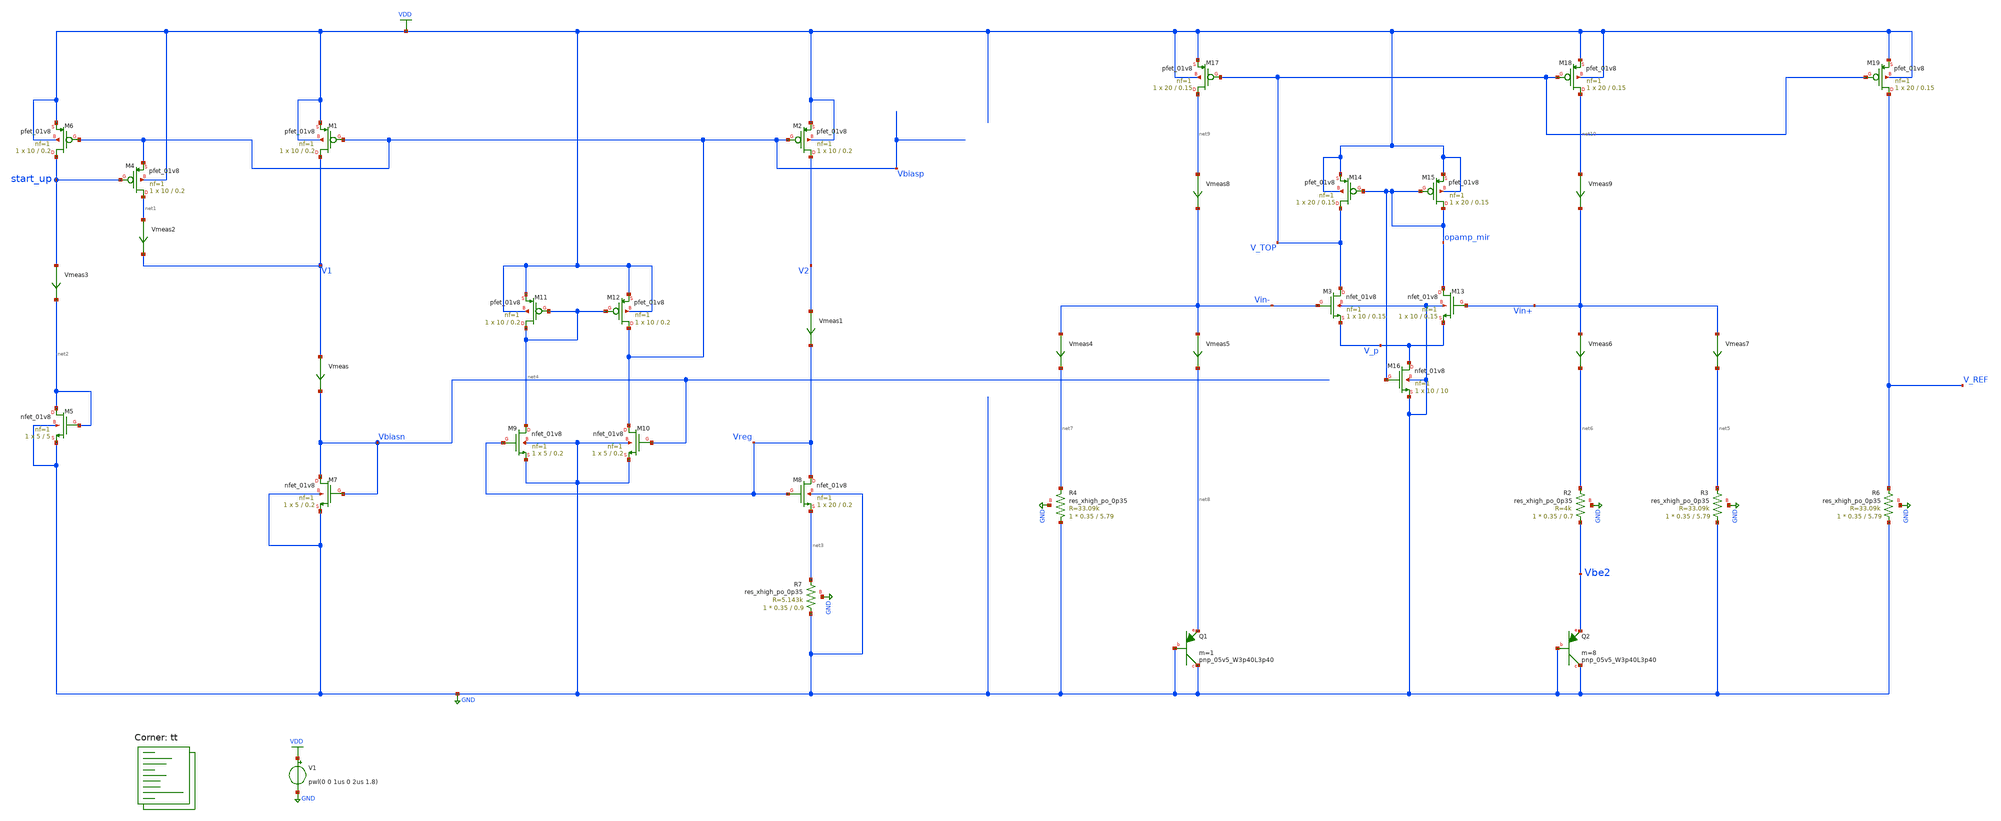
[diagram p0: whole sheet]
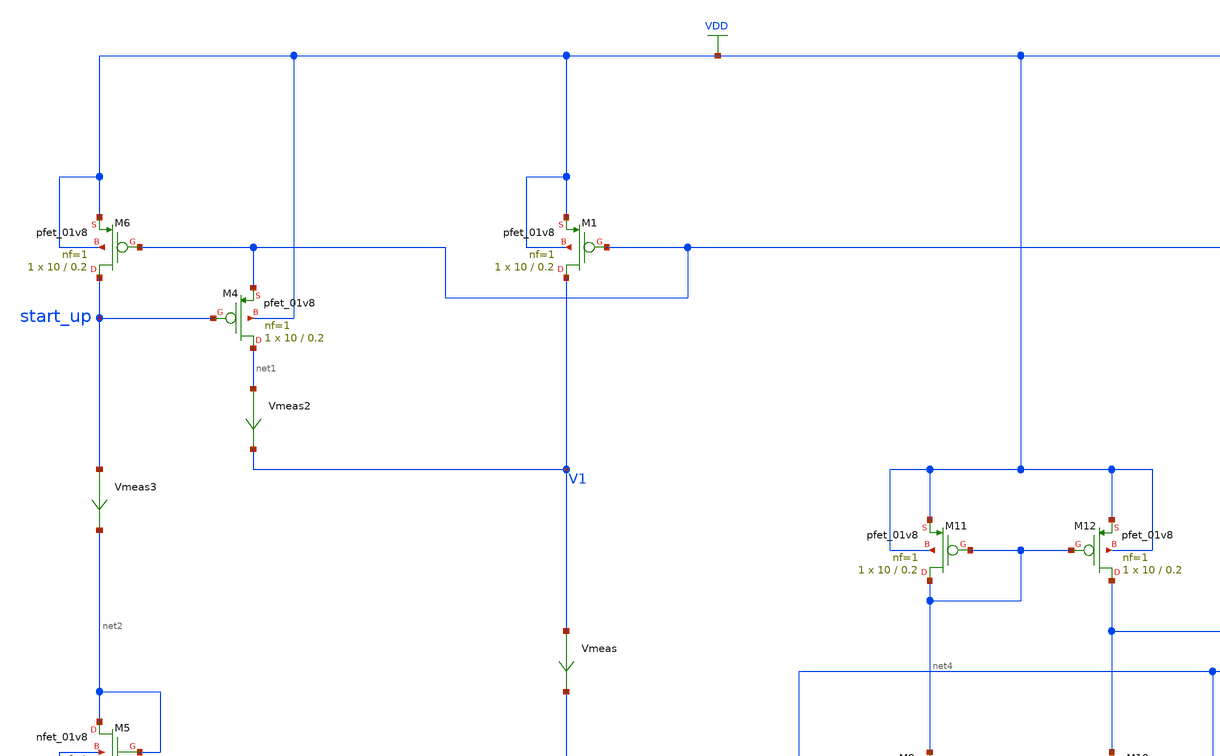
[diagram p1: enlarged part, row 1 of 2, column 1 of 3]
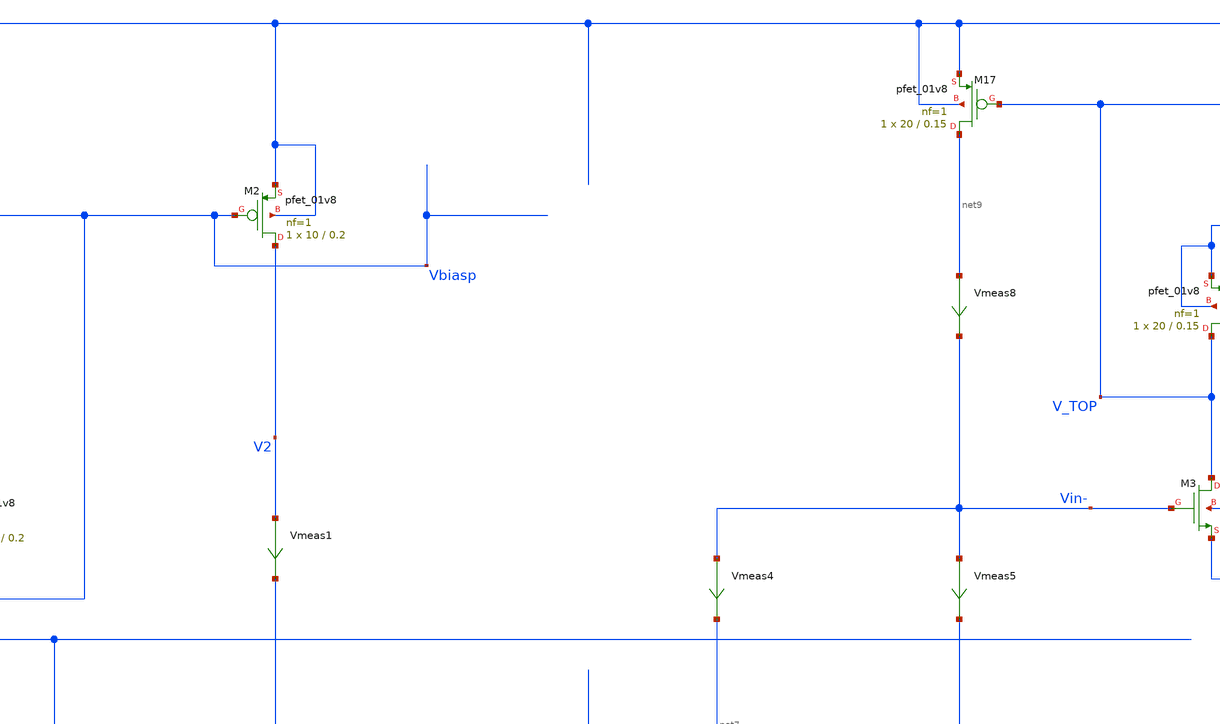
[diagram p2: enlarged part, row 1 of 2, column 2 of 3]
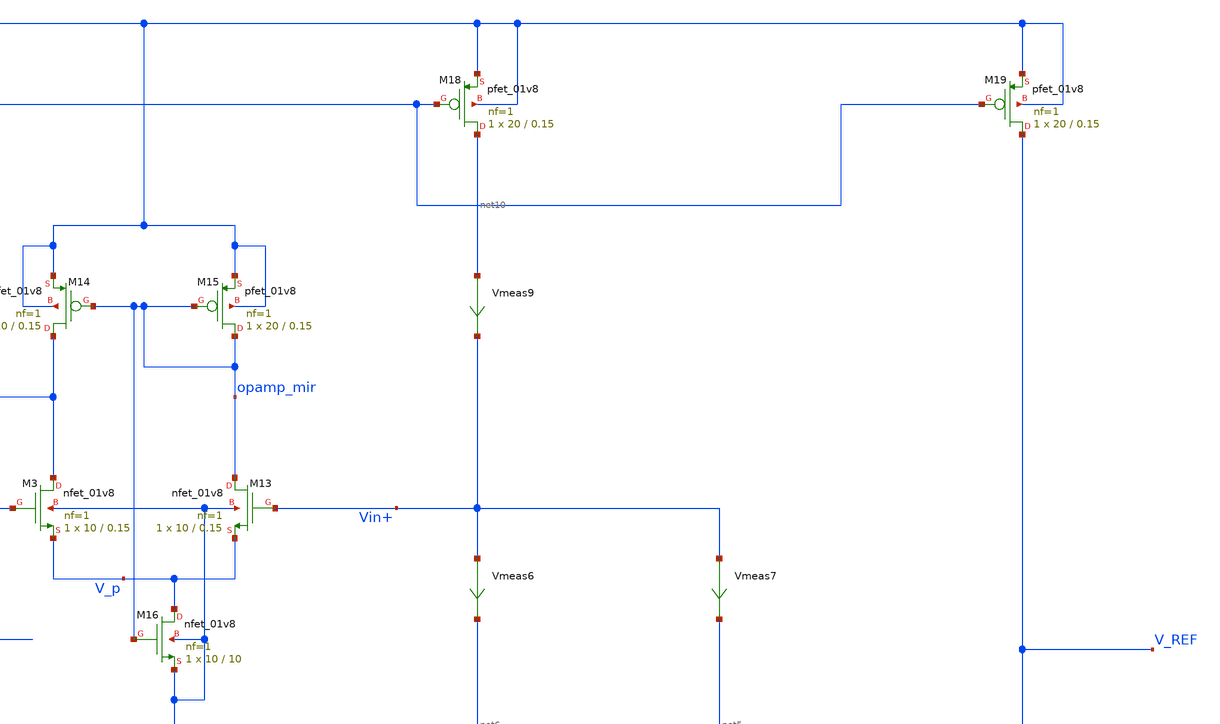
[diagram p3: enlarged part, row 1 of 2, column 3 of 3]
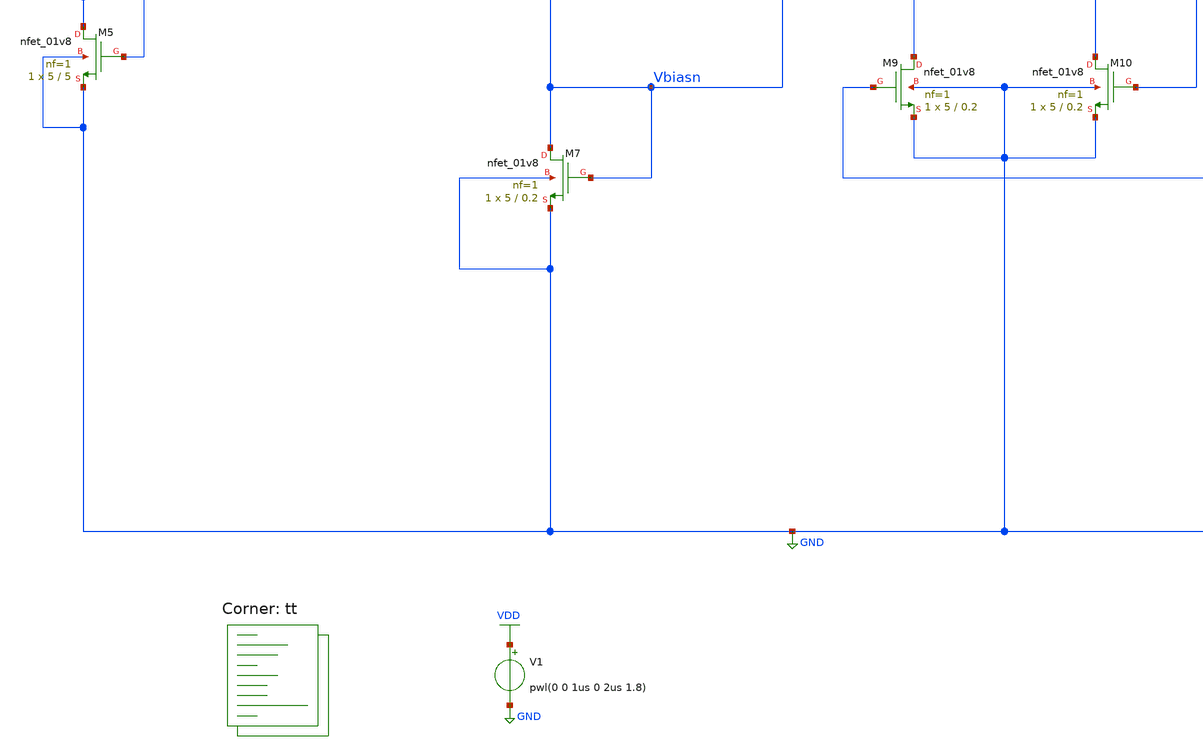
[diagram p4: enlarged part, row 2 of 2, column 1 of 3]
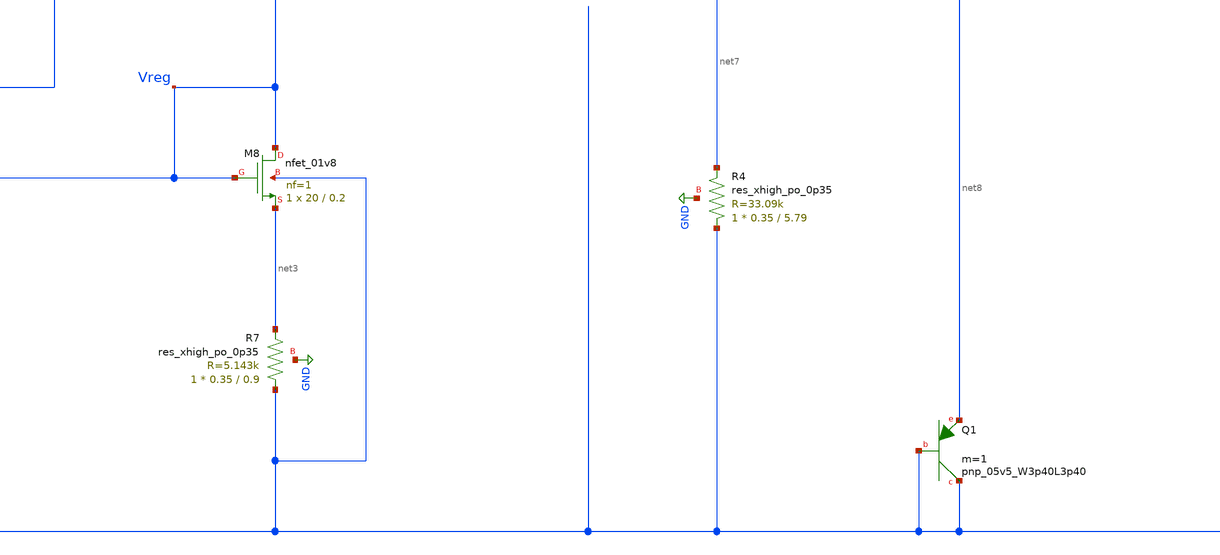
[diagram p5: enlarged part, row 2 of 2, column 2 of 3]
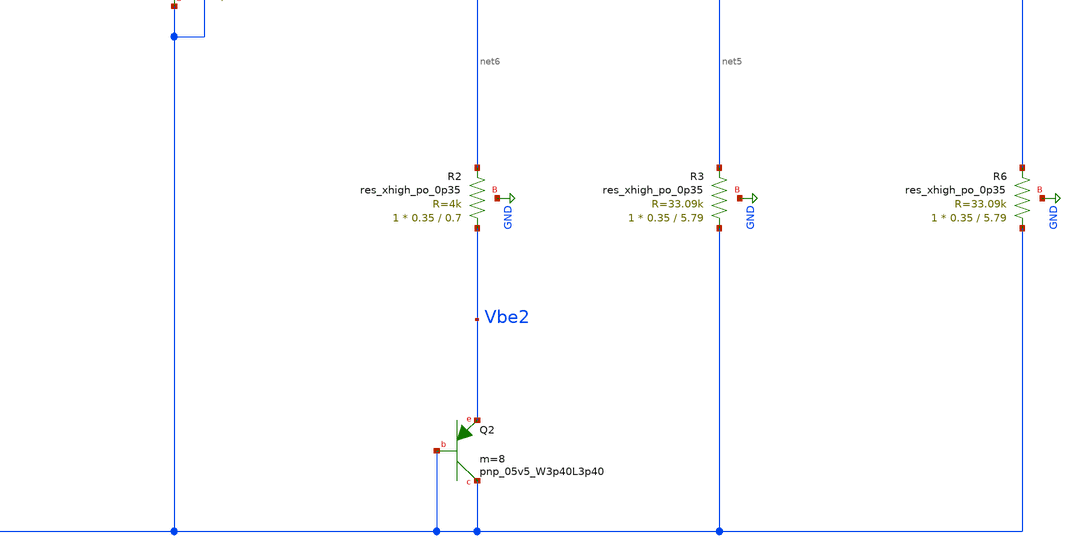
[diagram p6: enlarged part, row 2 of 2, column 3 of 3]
** sch_path: projects/bandgapref/xschem_ngspice/new_files/tb_low_voltage_BGR_8.sch
**.subckt tb_low_voltage_BGR_8
V1 VDD GND pwl(0 0 1us 0 2us 1.8)
XM1 V1 Vbiasp VDD VDD sky130_fd_pr__pfet_01v8 L=0.2 W=10 nf=1 ad='int((nf+1)/2) * W/nf * 0.29' as='int((nf+2)/2) * W/nf * 0.29'
+ pd='2*int((nf+1)/2) * (W/nf + 0.29)' ps='2*int((nf+2)/2) * (W/nf + 0.29)' nrd='0.29 / W' nrs='0.29 / W'
+ sa=0 sb=0 sd=0 mult=1 m=1
XM2 V2 Vbiasp VDD VDD sky130_fd_pr__pfet_01v8 L=0.2 W=10 nf=1 ad='int((nf+1)/2) * W/nf * 0.29' as='int((nf+2)/2) * W/nf * 0.29'
+ pd='2*int((nf+1)/2) * (W/nf + 0.29)' ps='2*int((nf+2)/2) * (W/nf + 0.29)' nrd='0.29 / W' nrs='0.29 / W'
+ sa=0 sb=0 sd=0 mult=1 m=1
Vmeas V1 Vbiasn 0
.save i(vmeas)
Vmeas1 V2 Vreg 0
.save i(vmeas1)
XM5 net2 net2 GND GND sky130_fd_pr__nfet_01v8 L=5 W=5 nf=1 ad='int((nf+1)/2) * W/nf * 0.29' as='int((nf+2)/2) * W/nf * 0.29'
+ pd='2*int((nf+1)/2) * (W/nf + 0.29)' ps='2*int((nf+2)/2) * (W/nf + 0.29)' nrd='0.29 / W' nrs='0.29 / W'
+ sa=0 sb=0 sd=0 mult=1 m=1
XM6 start_up Vbiasp VDD VDD sky130_fd_pr__pfet_01v8 L=0.2 W=10 nf=1 ad='int((nf+1)/2) * W/nf * 0.29'
+ as='int((nf+2)/2) * W/nf * 0.29' pd='2*int((nf+1)/2) * (W/nf + 0.29)' ps='2*int((nf+2)/2) * (W/nf + 0.29)'
+ nrd='0.29 / W' nrs='0.29 / W' sa=0 sb=0 sd=0 mult=1 m=1
XM4 net1 start_up Vbiasp VDD sky130_fd_pr__pfet_01v8 L=0.2 W=10 nf=1 ad='int((nf+1)/2) * W/nf * 0.29'
+ as='int((nf+2)/2) * W/nf * 0.29' pd='2*int((nf+1)/2) * (W/nf + 0.29)' ps='2*int((nf+2)/2) * (W/nf + 0.29)'
+ nrd='0.29 / W' nrs='0.29 / W' sa=0 sb=0 sd=0 mult=1 m=1
XM7 Vbiasn Vbiasn GND GND sky130_fd_pr__nfet_01v8 L=0.2 W=5 nf=1 ad='int((nf+1)/2) * W/nf * 0.29' as='int((nf+2)/2) * W/nf * 0.29'
+ pd='2*int((nf+1)/2) * (W/nf + 0.29)' ps='2*int((nf+2)/2) * (W/nf + 0.29)' nrd='0.29 / W' nrs='0.29 / W'
+ sa=0 sb=0 sd=0 mult=1 m=1
XM8 Vreg Vreg net3 GND sky130_fd_pr__nfet_01v8 L=0.2 W=20 nf=1 ad='int((nf+1)/2) * W/nf * 0.29' as='int((nf+2)/2) * W/nf * 0.29'
+ pd='2*int((nf+1)/2) * (W/nf + 0.29)' ps='2*int((nf+2)/2) * (W/nf + 0.29)' nrd='0.29 / W' nrs='0.29 / W'
+ sa=0 sb=0 sd=0 mult=1 m=1
Vmeas2 net1 V1 0
.save i(vmeas2)
Vmeas3 start_up net2 0
.save i(vmeas3)
XM9 net4 Vreg GND GND sky130_fd_pr__nfet_01v8 L=0.2 W=5 nf=1 ad='int((nf+1)/2) * W/nf * 0.29' as='int((nf+2)/2) * W/nf * 0.29'
+ pd='2*int((nf+1)/2) * (W/nf + 0.29)' ps='2*int((nf+2)/2) * (W/nf + 0.29)' nrd='0.29 / W' nrs='0.29 / W'
+ sa=0 sb=0 sd=0 mult=1 m=1
XM10 Vbiasp Vbiasn GND GND sky130_fd_pr__nfet_01v8 L=0.2 W=5 nf=1 ad='int((nf+1)/2) * W/nf * 0.29' as='int((nf+2)/2) * W/nf * 0.29'
+ pd='2*int((nf+1)/2) * (W/nf + 0.29)' ps='2*int((nf+2)/2) * (W/nf + 0.29)' nrd='0.29 / W' nrs='0.29 / W'
+ sa=0 sb=0 sd=0 mult=1 m=1
XM11 net4 net4 VDD VDD sky130_fd_pr__pfet_01v8 L=0.2 W=10 nf=1 ad='int((nf+1)/2) * W/nf * 0.29' as='int((nf+2)/2) * W/nf * 0.29'
+ pd='2*int((nf+1)/2) * (W/nf + 0.29)' ps='2*int((nf+2)/2) * (W/nf + 0.29)' nrd='0.29 / W' nrs='0.29 / W'
+ sa=0 sb=0 sd=0 mult=1 m=1
XM12 Vbiasp net4 VDD VDD sky130_fd_pr__pfet_01v8 L=0.2 W=10 nf=1 ad='int((nf+1)/2) * W/nf * 0.29' as='int((nf+2)/2) * W/nf * 0.29'
+ pd='2*int((nf+1)/2) * (W/nf + 0.29)' ps='2*int((nf+2)/2) * (W/nf + 0.29)' nrd='0.29 / W' nrs='0.29 / W'
+ sa=0 sb=0 sd=0 mult=1 m=1
XM3 V_TOP Vin- V_p GND sky130_fd_pr__nfet_01v8 L=0.15 W=10 nf=1 ad='int((nf+1)/2) * W/nf * 0.29' as='int((nf+2)/2) * W/nf * 0.29'
+ pd='2*int((nf+1)/2) * (W/nf + 0.29)' ps='2*int((nf+2)/2) * (W/nf + 0.29)' nrd='0.29 / W' nrs='0.29 / W'
+ sa=0 sb=0 sd=0 mult=1 m=1
XM13 opamp_mir Vin+ V_p GND sky130_fd_pr__nfet_01v8 L=0.15 W=10 nf=1 ad='int((nf+1)/2) * W/nf * 0.29'
+ as='int((nf+2)/2) * W/nf * 0.29' pd='2*int((nf+1)/2) * (W/nf + 0.29)' ps='2*int((nf+2)/2) * (W/nf + 0.29)'
+ nrd='0.29 / W' nrs='0.29 / W' sa=0 sb=0 sd=0 mult=1 m=1
XM14 V_TOP opamp_mir VDD VDD sky130_fd_pr__pfet_01v8 L=0.15 W=20 nf=1 ad='int((nf+1)/2) * W/nf * 0.29'
+ as='int((nf+2)/2) * W/nf * 0.29' pd='2*int((nf+1)/2) * (W/nf + 0.29)' ps='2*int((nf+2)/2) * (W/nf + 0.29)'
+ nrd='0.29 / W' nrs='0.29 / W' sa=0 sb=0 sd=0 mult=1 m=1
XM15 opamp_mir opamp_mir VDD VDD sky130_fd_pr__pfet_01v8 L=0.15 W=20 nf=1 ad='int((nf+1)/2) * W/nf * 0.29'
+ as='int((nf+2)/2) * W/nf * 0.29' pd='2*int((nf+1)/2) * (W/nf + 0.29)' ps='2*int((nf+2)/2) * (W/nf + 0.29)'
+ nrd='0.29 / W' nrs='0.29 / W' sa=0 sb=0 sd=0 mult=1 m=1
XQ1 GND GND net8 sky130_fd_pr__pnp_05v5_W3p40L3p40 m=1
XQ2 GND GND Vbe2 sky130_fd_pr__pnp_05v5_W3p40L3p40 m=8
XR2 Vbe2 net6 GND sky130_fd_pr__res_xhigh_po_0p35 L=0.7 mult=1 m=1
XM17 net9 V_TOP VDD VDD sky130_fd_pr__pfet_01v8 L=0.15 W=20 nf=1 ad='int((nf+1)/2) * W/nf * 0.29' as='int((nf+2)/2) * W/nf * 0.29'
+ pd='2*int((nf+1)/2) * (W/nf + 0.29)' ps='2*int((nf+2)/2) * (W/nf + 0.29)' nrd='0.29 / W' nrs='0.29 / W'
+ sa=0 sb=0 sd=0 mult=1 m=1
XM18 net10 V_TOP VDD VDD sky130_fd_pr__pfet_01v8 L=0.15 W=20 nf=1 ad='int((nf+1)/2) * W/nf * 0.29' as='int((nf+2)/2) * W/nf * 0.29'
+ pd='2*int((nf+1)/2) * (W/nf + 0.29)' ps='2*int((nf+2)/2) * (W/nf + 0.29)' nrd='0.29 / W' nrs='0.29 / W'
+ sa=0 sb=0 sd=0 mult=1 m=1
XR3 GND net5 GND sky130_fd_pr__res_xhigh_po_0p35 L=5.79 mult=1 m=1
XR4 GND net7 GND sky130_fd_pr__res_xhigh_po_0p35 L=5.79 mult=1 m=1
XM19 V_REF V_TOP VDD VDD sky130_fd_pr__pfet_01v8 L=0.15 W=20 nf=1 ad='int((nf+1)/2) * W/nf * 0.29' as='int((nf+2)/2) * W/nf * 0.29'
+ pd='2*int((nf+1)/2) * (W/nf + 0.29)' ps='2*int((nf+2)/2) * (W/nf + 0.29)' nrd='0.29 / W' nrs='0.29 / W'
+ sa=0 sb=0 sd=0 mult=1 m=1
XR6 GND V_REF GND sky130_fd_pr__res_xhigh_po_0p35 L=5.79 mult=1 m=1
Vmeas4 Vin- net7 0
.save i(vmeas4)
Vmeas5 Vin- net8 0
.save i(vmeas5)
Vmeas6 Vin+ net6 0
.save i(vmeas6)
Vmeas7 Vin+ net5 0
.save i(vmeas7)
Vmeas8 net9 Vin- 0
.save i(vmeas8)
Vmeas9 net10 Vin+ 0
.save i(vmeas9)
XR7 GND net3 GND sky130_fd_pr__res_xhigh_po_0p35 L=0.9 mult=1 m=1
XM16 V_p opamp_mir GND GND sky130_fd_pr__nfet_01v8 L=10 W=10 nf=1 ad='int((nf+1)/2) * W/nf * 0.29' as='int((nf+2)/2) * W/nf * 0.29'
+ pd='2*int((nf+1)/2) * (W/nf + 0.29)' ps='2*int((nf+2)/2) * (W/nf + 0.29)' nrd='0.29 / W' nrs='0.29 / W'
+ sa=0 sb=0 sd=0 mult=1 m=1
**** begin user architecture code
.lib $::SKYWATER_MODELS/sky130.lib.spice tt



.option method=gear
.option wnflag=1
.option savecurrents
* .temp =140

.save @m.xm1.msky130_fd_pr__pfet_01v8[gm] @m.xm1.msky130_fd_pr__pfet_01v8[vth] @m.xm1.msky130_fd_pr__pfet_01v8[vgs] @m.xm1.msky130_fd_pr__pfet_01v8[vds] @m.xm2.msky130_fd_pr__pfet_01v8[gm] @m.xm2.msky130_fd_pr__pfet_01v8[vth] @m.xm2.msky130_fd_pr__pfet_01v8[vgs] @m.xm2.msky130_fd_pr__pfet_01v8[vds] @m.xm3.msky130_fd_pr__pfet_01v8[gm] @m.xm4.msky130_fd_pr__pfet_01v8[gm] @m.xm4.msky130_fd_pr__nfet_01v8[gm] @m.x1.xm1.msky130_fd_pr__nfet_01v8[gm] @m.x1.xm2.msky130_fd_pr__nfet_01v8[gm] @m.x1.xm3.msky130_fd_pr__nfet_01v8[gm] @m.x1.xm4.msky130_fd_pr__pfet_01v8[gm] @m.x1.xm5.msky130_fd_pr__pfet_01v8[gm] @m.x1.xm6.msky130_fd_pr__nfet_01v8[gm] @m.x1.xm7.msky130_fd_pr__pfet_01v8[gm] @m.x2.xm1.msky130_fd_pr__nfet_01v8[gm] @m.x2.xm2.msky130_fd_pr__nfet_01v8[gm] @m.x2.xm3.msky130_fd_pr__nfet_01v8[gm] @m.x2.xm4.msky130_fd_pr__pfet_01v8[gm] @m.x2.xm5.msky130_fd_pr__pfet_01v8[gm] @m.x2.xm6.msky130_fd_pr__pfet_01v8[gm] @m.x2.xm7.msky130_fd_pr__pfet_01v8[gm]

* .ic v(vin-) = 0.8
* .ic v(vin+) = 0.8
* .ic v(v_top) = 1.8

.control

  * let start_vdd = 0.3
  * let stop_vdd = 1.8
  * let delta_vdd = 0.3
  * let w_act = start_vdd
  * while w_act le stop_vdd
    * echo $&w_act
    * alter V1 = w_act
    * echo v[vdd]
    * alter @V1[pwl] = [ 0 0 1us 0 2us $&w_act ]
    * reset
    save all
    * run
    * dc temp -40 120 5 V1 1.6 2.0 0.05
    * dc V1 1.7 1.9 0.001 temp -40 120 40
    * dc V1 0 2.0 0.01 temp -40 120 40
    * dc V1 0 2.0 0.01
    tran 1ns 8us
    remzerovec
    write tb_low_voltage_BGR_8.raw
    * let w_act = w_act + delta_vdd
    set appendwrite
  * end

.endc



**** end user architecture code
**.ends
.GLOBAL GND
.GLOBAL VDD
.end
